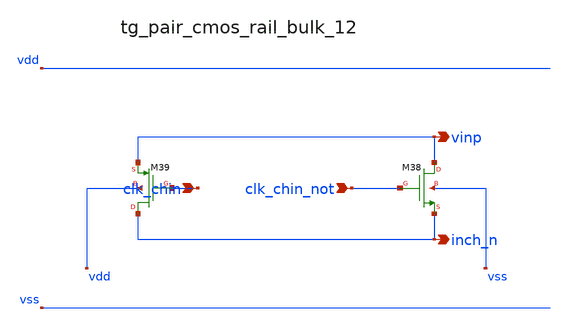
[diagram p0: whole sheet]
** sch_path: analog-db/raw/ia_003_fan_chopper_pf/hier/blocks/tg_pair_cmos_rail_bulk_12.sch
**.subckt tg_pair_cmos_rail_bulk_12 clk_chin clk_chin_not vinp inch_n
*.ipin clk_chin
*.ipin clk_chin_not
*.opin vinp
*.opin inch_n
XM38 vinp clk_chin_not inch_n vss sg13_lv_nmos w=x_dut_xm38_w l=x_dut_xm38_l ng=1 m=x_dut_xm38_m
XM39 inch_n clk_chin vinp vdd sg13_lv_pmos w=x_dut_xm39_w l=x_dut_xm39_l ng=1 m=x_dut_xm39_m
**.ends
.end
